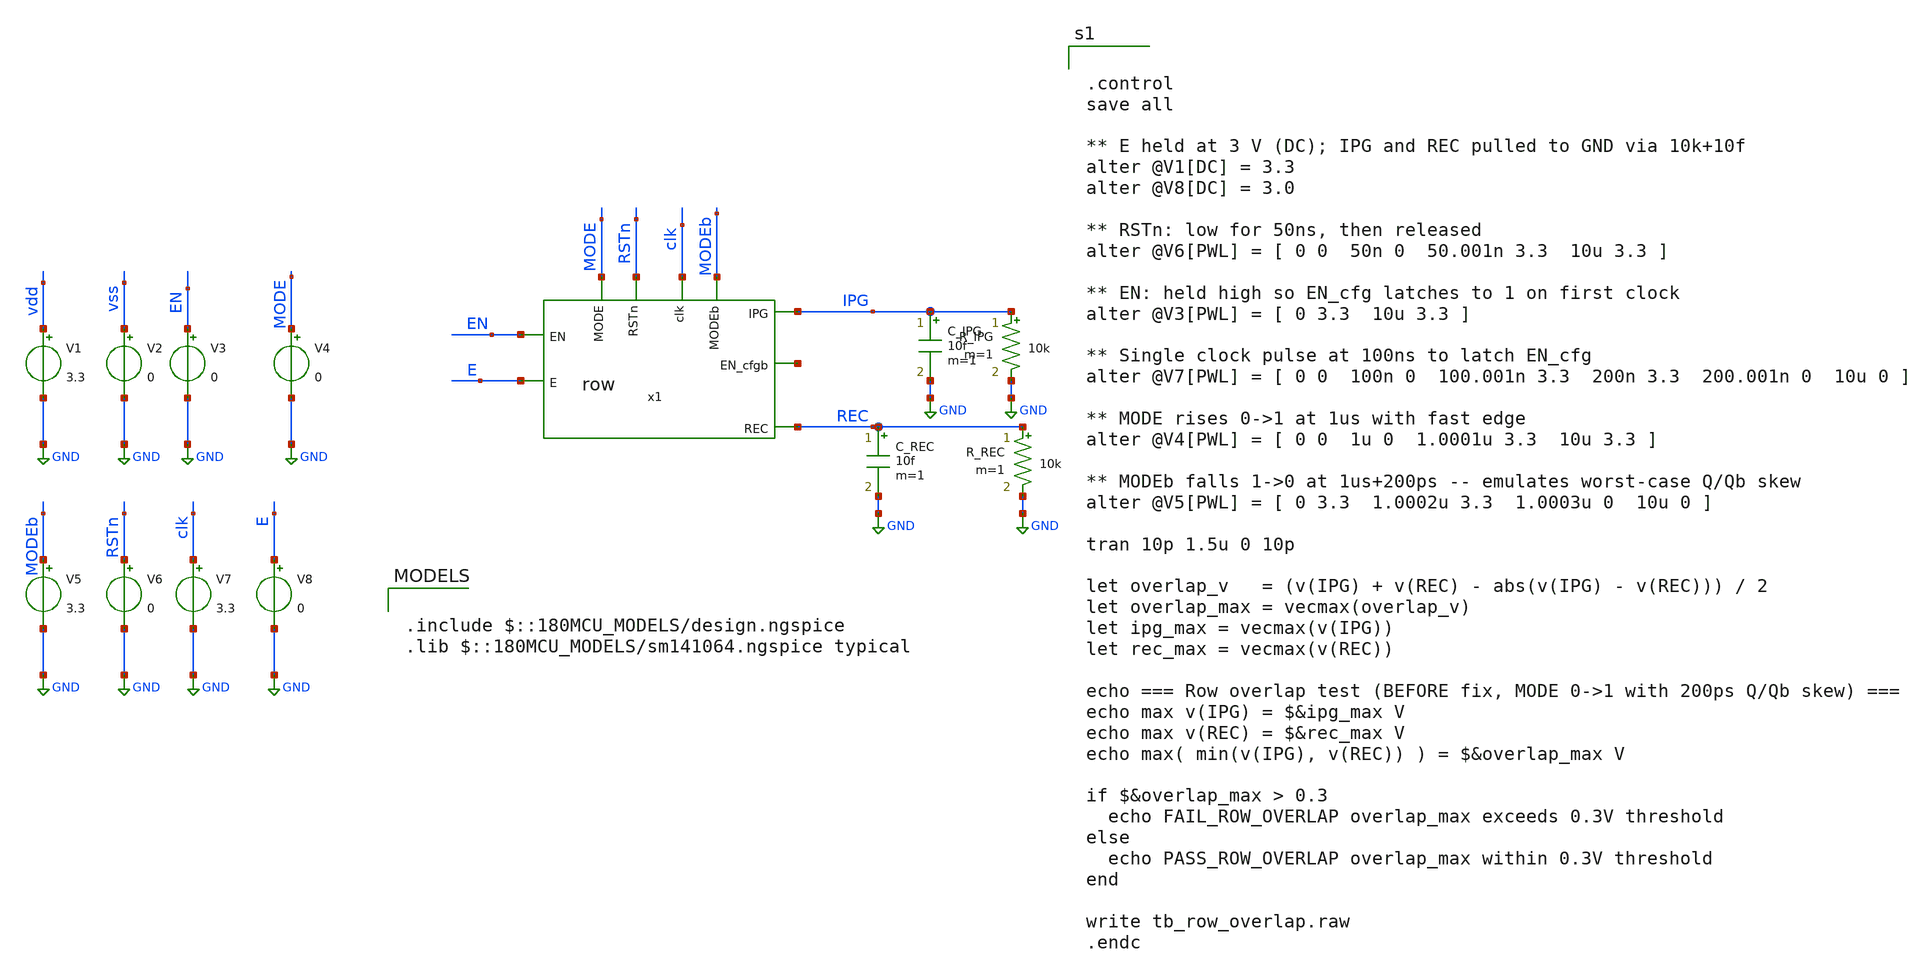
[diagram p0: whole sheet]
** sch_path: tb_row_overlap.sch
**.subckt tb_row_overlap
x1 IPG MODEb EN net1 clk E MODE RSTn REC row
V1 vdd GND 3.3
V2 vss GND 0
V3 EN GND 0
V4 MODE GND 0
V5 MODEb GND 3.3
V6 RSTn GND 0
V7 clk GND 3.3
V8 E GND 0
C_REC REC GND 10f m=1
C_IPG IPG GND 10f m=1
R_IPG IPG GND 10k m=1
R_REC REC GND 10k m=1
**** begin user architecture code

.include $::180MCU_MODELS/design.ngspice
.lib $::180MCU_MODELS/sm141064.ngspice typical



.control
save all

** E held at 3 V (DC); IPG and REC pulled to GND via 10k+10f
alter @V1[DC] = 3.3
alter @V8[DC] = 3.0

** RSTn: low for 50ns, then released
alter @V6[PWL] = [ 0 0  50n 0  50.001n 3.3  10u 3.3 ]

** EN: held high so EN_cfg latches to 1 on first clock
alter @V3[PWL] = [ 0 3.3  10u 3.3 ]

** Single clock pulse at 100ns to latch EN_cfg
alter @V7[PWL] = [ 0 0  100n 0  100.001n 3.3  200n 3.3  200.001n 0  10u 0 ]

** MODE rises 0->1 at 1us with fast edge
alter @V4[PWL] = [ 0 0  1u 0  1.0001u 3.3  10u 3.3 ]

** MODEb falls 1->0 at 1us+200ps -- emulates worst-case Q/Qb skew
alter @V5[PWL] = [ 0 3.3  1.0002u 3.3  1.0003u 0  10u 0 ]

tran 10p 1.5u 0 10p

let overlap_v   = (v(IPG) + v(REC) - abs(v(IPG) - v(REC))) / 2
let overlap_max = vecmax(overlap_v)
let ipg_max = vecmax(v(IPG))
let rec_max = vecmax(v(REC))

echo === Row overlap test (BEFORE fix, MODE 0->1 with 200ps Q/Qb skew) ===
echo max v(IPG) = $&ipg_max V
echo max v(REC) = $&rec_max V
echo max( min(v(IPG), v(REC)) ) = $&overlap_max V

if $&overlap_max > 0.3
  echo FAIL_ROW_OVERLAP overlap_max exceeds 0.3V threshold
else
  echo PASS_ROW_OVERLAP overlap_max within 0.3V threshold
end

write tb_row_overlap.raw
.endc


**** end user architecture code
**.ends

* expanding   symbol:  row.sym # of pins=9
** sym_path: row.sym
** sch_path: row.sch
.subckt row IPG MODEb EN EN_cfgb clk E MODE RSTn REC
*.ipin EN
*.ipin clk
*.ipin MODEb
*.ipin MODE
*.ipin E
*.opin IPG
*.opin REC
*.ipin RSTn
*.opin EN_cfgb
x1 EN_cfg SW_IPG MODEb AND
x2 vdd RSTn EN EN_cfg EN_cfgb clk GND DFF
x3 IPG SW_IPG SW_IPGb E TGATE
x4 EN_cfg SW_REC MODE AND
x6 REC SW_REC SW_RECb E TGATE
x5 SW_IPGb SW_IPG INV
x7 SW_RECb SW_REC INV
.ends


* expanding   symbol:  AND/AND.sym # of pins=3
** sym_path: AND/AND.sym
** sch_path: AND/AND.sch
.subckt AND IN0 OUT IN1
*.opin OUT
*.ipin IN0
*.ipin IN1
XM1 net1 IN0 net2 GND nfet_03v3 L=0.28u W=1u nf=1 ad='int((nf+1)/2) * W/nf * 0.18u' as='int((nf+2)/2) * W/nf * 0.18u'
+ pd='2*int((nf+1)/2) * (W/nf + 0.18u)' ps='2*int((nf+2)/2) * (W/nf + 0.18u)' nrd='0.18u / W' nrs='0.18u / W'
+ sa=0 sb=0 sd=0 m=1
XM2 net2 IN1 GND GND nfet_03v3 L=0.28u W=1u nf=1 ad='int((nf+1)/2) * W/nf * 0.18u' as='int((nf+2)/2) * W/nf * 0.18u'
+ pd='2*int((nf+1)/2) * (W/nf + 0.18u)' ps='2*int((nf+2)/2) * (W/nf + 0.18u)' nrd='0.18u / W' nrs='0.18u / W'
+ sa=0 sb=0 sd=0 m=1
XM3 net1 IN0 vdd vdd pfet_03v3 L=0.28u W=1u nf=1 ad='int((nf+1)/2) * W/nf * 0.18u' as='int((nf+2)/2) * W/nf * 0.18u'
+ pd='2*int((nf+1)/2) * (W/nf + 0.18u)' ps='2*int((nf+2)/2) * (W/nf + 0.18u)' nrd='0.18u / W' nrs='0.18u / W'
+ sa=0 sb=0 sd=0 m=1
XM4 net1 IN1 vdd vdd pfet_03v3 L=0.28u W=1u nf=1 ad='int((nf+1)/2) * W/nf * 0.18u' as='int((nf+2)/2) * W/nf * 0.18u'
+ pd='2*int((nf+1)/2) * (W/nf + 0.18u)' ps='2*int((nf+2)/2) * (W/nf + 0.18u)' nrd='0.18u / W' nrs='0.18u / W'
+ sa=0 sb=0 sd=0 m=1
x1 OUT net1 INV
.ends


* expanding   symbol:  DFF/DFF.sym # of pins=7
** sym_path: DFF/DFF.sym
** sch_path: DFF/DFF.sch
.subckt DFF vdd RSTn D Q Qb CLK vss
*.ipin D
*.ipin CLK
*.ipin RSTn
*.opin Q
*.iopin vdd
*.iopin vss
*.opin Qb
XM1 net1 D net3 vss nfet_03v3 L=0.28u W=1u nf=1 ad='int((nf+1)/2) * W/nf * 0.18u' as='int((nf+2)/2) * W/nf * 0.18u'
+ pd='2*int((nf+1)/2) * (W/nf + 0.18u)' ps='2*int((nf+2)/2) * (W/nf + 0.18u)' nrd='0.18u / W' nrs='0.18u / W'
+ sa=0 sb=0 sd=0 m=1
XM2 net1 D net2 vdd pfet_03v3 L=0.28u W=1u nf=1 ad='int((nf+1)/2) * W/nf * 0.18u' as='int((nf+2)/2) * W/nf * 0.18u'
+ pd='2*int((nf+1)/2) * (W/nf + 0.18u)' ps='2*int((nf+2)/2) * (W/nf + 0.18u)' nrd='0.18u / W' nrs='0.18u / W'
+ sa=0 sb=0 sd=0 m=1
XM3 net2 c vdd vdd pfet_03v3 L=0.28u W=1u nf=1 ad='int((nf+1)/2) * W/nf * 0.18u' as='int((nf+2)/2) * W/nf * 0.18u'
+ pd='2*int((nf+1)/2) * (W/nf + 0.18u)' ps='2*int((nf+2)/2) * (W/nf + 0.18u)' nrd='0.18u / W' nrs='0.18u / W'
+ sa=0 sb=0 sd=0 m=1
XM4 net3 cbar vss vss nfet_03v3 L=0.28u W=1u nf=1 ad='int((nf+1)/2) * W/nf * 0.18u' as='int((nf+2)/2) * W/nf * 0.18u'
+ pd='2*int((nf+1)/2) * (W/nf + 0.18u)' ps='2*int((nf+2)/2) * (W/nf + 0.18u)' nrd='0.18u / W' nrs='0.18u / W'
+ sa=0 sb=0 sd=0 m=1
XM5 cbar CLK vss vss nfet_03v3 L=0.28u W=1u nf=1 ad='int((nf+1)/2) * W/nf * 0.18u' as='int((nf+2)/2) * W/nf * 0.18u'
+ pd='2*int((nf+1)/2) * (W/nf + 0.18u)' ps='2*int((nf+2)/2) * (W/nf + 0.18u)' nrd='0.18u / W' nrs='0.18u / W'
+ sa=0 sb=0 sd=0 m=1
XM6 cbar CLK vdd vdd pfet_03v3 L=0.28u W=1u nf=1 ad='int((nf+1)/2) * W/nf * 0.18u' as='int((nf+2)/2) * W/nf * 0.18u'
+ pd='2*int((nf+1)/2) * (W/nf + 0.18u)' ps='2*int((nf+2)/2) * (W/nf + 0.18u)' nrd='0.18u / W' nrs='0.18u / W'
+ sa=0 sb=0 sd=0 m=1
XM7 c cbar vss vss nfet_03v3 L=0.28u W=1u nf=1 ad='int((nf+1)/2) * W/nf * 0.18u' as='int((nf+2)/2) * W/nf * 0.18u'
+ pd='2*int((nf+1)/2) * (W/nf + 0.18u)' ps='2*int((nf+2)/2) * (W/nf + 0.18u)' nrd='0.18u / W' nrs='0.18u / W'
+ sa=0 sb=0 sd=0 m=1
XM8 c cbar vdd vdd pfet_03v3 L=0.28u W=1u nf=1 ad='int((nf+1)/2) * W/nf * 0.18u' as='int((nf+2)/2) * W/nf * 0.18u'
+ pd='2*int((nf+1)/2) * (W/nf + 0.18u)' ps='2*int((nf+2)/2) * (W/nf + 0.18u)' nrd='0.18u / W' nrs='0.18u / W'
+ sa=0 sb=0 sd=0 m=1
XM11 net5 RSTn net4 vss nfet_03v3 L=0.28u W=1u nf=1 ad='int((nf+1)/2) * W/nf * 0.18u' as='int((nf+2)/2) * W/nf * 0.18u'
+ pd='2*int((nf+1)/2) * (W/nf + 0.18u)' ps='2*int((nf+2)/2) * (W/nf + 0.18u)' nrd='0.18u / W' nrs='0.18u / W'
+ sa=0 sb=0 sd=0 m=1
XM12 net4 net6 vss vss nfet_03v3 L=0.28u W=1u nf=1 ad='int((nf+1)/2) * W/nf * 0.18u' as='int((nf+2)/2) * W/nf * 0.18u'
+ pd='2*int((nf+1)/2) * (W/nf + 0.18u)' ps='2*int((nf+2)/2) * (W/nf + 0.18u)' nrd='0.18u / W' nrs='0.18u / W'
+ sa=0 sb=0 sd=0 m=1
XM13 net5 RSTn vdd vdd pfet_03v3 L=0.28u W=1u nf=1 ad='int((nf+1)/2) * W/nf * 0.18u' as='int((nf+2)/2) * W/nf * 0.18u'
+ pd='2*int((nf+1)/2) * (W/nf + 0.18u)' ps='2*int((nf+2)/2) * (W/nf + 0.18u)' nrd='0.18u / W' nrs='0.18u / W'
+ sa=0 sb=0 sd=0 m=1
XM14 net5 net6 vdd vdd pfet_03v3 L=0.28u W=1u nf=1 ad='int((nf+1)/2) * W/nf * 0.18u' as='int((nf+2)/2) * W/nf * 0.18u'
+ pd='2*int((nf+1)/2) * (W/nf + 0.18u)' ps='2*int((nf+2)/2) * (W/nf + 0.18u)' nrd='0.18u / W' nrs='0.18u / W'
+ sa=0 sb=0 sd=0 m=1
XM15 net6 net1 vss vss nfet_03v3 L=0.28u W=1u nf=1 ad='int((nf+1)/2) * W/nf * 0.18u' as='int((nf+2)/2) * W/nf * 0.18u'
+ pd='2*int((nf+1)/2) * (W/nf + 0.18u)' ps='2*int((nf+2)/2) * (W/nf + 0.18u)' nrd='0.18u / W' nrs='0.18u / W'
+ sa=0 sb=0 sd=0 m=1
XM16 net6 net1 vdd vdd pfet_03v3 L=0.28u W=1u nf=1 ad='int((nf+1)/2) * W/nf * 0.18u' as='int((nf+2)/2) * W/nf * 0.18u'
+ pd='2*int((nf+1)/2) * (W/nf + 0.18u)' ps='2*int((nf+2)/2) * (W/nf + 0.18u)' nrd='0.18u / W' nrs='0.18u / W'
+ sa=0 sb=0 sd=0 m=1
XM21 net9 net7 net8 vss nfet_03v3 L=0.28u W=1u nf=1 ad='int((nf+1)/2) * W/nf * 0.18u' as='int((nf+2)/2) * W/nf * 0.18u'
+ pd='2*int((nf+1)/2) * (W/nf + 0.18u)' ps='2*int((nf+2)/2) * (W/nf + 0.18u)' nrd='0.18u / W' nrs='0.18u / W'
+ sa=0 sb=0 sd=0 m=1
XM22 net8 RSTn vss vss nfet_03v3 L=0.28u W=1u nf=1 ad='int((nf+1)/2) * W/nf * 0.18u' as='int((nf+2)/2) * W/nf * 0.18u'
+ pd='2*int((nf+1)/2) * (W/nf + 0.18u)' ps='2*int((nf+2)/2) * (W/nf + 0.18u)' nrd='0.18u / W' nrs='0.18u / W'
+ sa=0 sb=0 sd=0 m=1
XM23 net9 net7 vdd vdd pfet_03v3 L=0.28u W=1u nf=1 ad='int((nf+1)/2) * W/nf * 0.18u' as='int((nf+2)/2) * W/nf * 0.18u'
+ pd='2*int((nf+1)/2) * (W/nf + 0.18u)' ps='2*int((nf+2)/2) * (W/nf + 0.18u)' nrd='0.18u / W' nrs='0.18u / W'
+ sa=0 sb=0 sd=0 m=1
XM24 net9 RSTn vdd vdd pfet_03v3 L=0.28u W=1u nf=1 ad='int((nf+1)/2) * W/nf * 0.18u' as='int((nf+2)/2) * W/nf * 0.18u'
+ pd='2*int((nf+1)/2) * (W/nf + 0.18u)' ps='2*int((nf+2)/2) * (W/nf + 0.18u)' nrd='0.18u / W' nrs='0.18u / W'
+ sa=0 sb=0 sd=0 m=1
XM25 Q net9 vss vss nfet_03v3 L=0.28u W=1u nf=1 ad='int((nf+1)/2) * W/nf * 0.18u' as='int((nf+2)/2) * W/nf * 0.18u'
+ pd='2*int((nf+1)/2) * (W/nf + 0.18u)' ps='2*int((nf+2)/2) * (W/nf + 0.18u)' nrd='0.18u / W' nrs='0.18u / W'
+ sa=0 sb=0 sd=0 m=1
XM26 Q net9 vdd vdd pfet_03v3 L=0.28u W=1u nf=1 ad='int((nf+1)/2) * W/nf * 0.18u' as='int((nf+2)/2) * W/nf * 0.18u'
+ pd='2*int((nf+1)/2) * (W/nf + 0.18u)' ps='2*int((nf+2)/2) * (W/nf + 0.18u)' nrd='0.18u / W' nrs='0.18u / W'
+ sa=0 sb=0 sd=0 m=1
XM19 net7 net9 net11 vss nfet_03v3 L=0.28u W=1u nf=1 ad='int((nf+1)/2) * W/nf * 0.18u' as='int((nf+2)/2) * W/nf * 0.18u'
+ pd='2*int((nf+1)/2) * (W/nf + 0.18u)' ps='2*int((nf+2)/2) * (W/nf + 0.18u)' nrd='0.18u / W' nrs='0.18u / W'
+ sa=0 sb=0 sd=0 m=1
XM20 net7 net9 net10 vdd pfet_03v3 L=0.28u W=1u nf=1 ad='int((nf+1)/2) * W/nf * 0.18u' as='int((nf+2)/2) * W/nf * 0.18u'
+ pd='2*int((nf+1)/2) * (W/nf + 0.18u)' ps='2*int((nf+2)/2) * (W/nf + 0.18u)' nrd='0.18u / W' nrs='0.18u / W'
+ sa=0 sb=0 sd=0 m=1
XM31 net10 c vdd vdd pfet_03v3 L=0.28u W=1u nf=1 ad='int((nf+1)/2) * W/nf * 0.18u' as='int((nf+2)/2) * W/nf * 0.18u'
+ pd='2*int((nf+1)/2) * (W/nf + 0.18u)' ps='2*int((nf+2)/2) * (W/nf + 0.18u)' nrd='0.18u / W' nrs='0.18u / W'
+ sa=0 sb=0 sd=0 m=1
XM32 net11 cbar vss vss nfet_03v3 L=0.28u W=1u nf=1 ad='int((nf+1)/2) * W/nf * 0.18u' as='int((nf+2)/2) * W/nf * 0.18u'
+ pd='2*int((nf+1)/2) * (W/nf + 0.18u)' ps='2*int((nf+2)/2) * (W/nf + 0.18u)' nrd='0.18u / W' nrs='0.18u / W'
+ sa=0 sb=0 sd=0 m=1
XM35 net12 net9 vss vss nfet_03v3 L=0.28u W=1u nf=1 ad='int((nf+1)/2) * W/nf * 0.18u' as='int((nf+2)/2) * W/nf * 0.18u'
+ pd='2*int((nf+1)/2) * (W/nf + 0.18u)' ps='2*int((nf+2)/2) * (W/nf + 0.18u)' nrd='0.18u / W' nrs='0.18u / W'
+ sa=0 sb=0 sd=0 m=1
XM36 net12 net9 vdd vdd pfet_03v3 L=0.28u W=1u nf=1 ad='int((nf+1)/2) * W/nf * 0.18u' as='int((nf+2)/2) * W/nf * 0.18u'
+ pd='2*int((nf+1)/2) * (W/nf + 0.18u)' ps='2*int((nf+2)/2) * (W/nf + 0.18u)' nrd='0.18u / W' nrs='0.18u / W'
+ sa=0 sb=0 sd=0 m=1
XM37 Qb net12 vss vss nfet_03v3 L=0.28u W=1u nf=1 ad='int((nf+1)/2) * W/nf * 0.18u' as='int((nf+2)/2) * W/nf * 0.18u'
+ pd='2*int((nf+1)/2) * (W/nf + 0.18u)' ps='2*int((nf+2)/2) * (W/nf + 0.18u)' nrd='0.18u / W' nrs='0.18u / W'
+ sa=0 sb=0 sd=0 m=1
XM38 Qb net12 vdd vdd pfet_03v3 L=0.28u W=1u nf=1 ad='int((nf+1)/2) * W/nf * 0.18u' as='int((nf+2)/2) * W/nf * 0.18u'
+ pd='2*int((nf+1)/2) * (W/nf + 0.18u)' ps='2*int((nf+2)/2) * (W/nf + 0.18u)' nrd='0.18u / W' nrs='0.18u / W'
+ sa=0 sb=0 sd=0 m=1
XM9 net1 c net5 vss nfet_03v3 L=0.28u W=1u nf=1 ad='int((nf+1)/2) * W/nf * 0.18u' as='int((nf+2)/2) * W/nf * 0.18u'
+ pd='2*int((nf+1)/2) * (W/nf + 0.18u)' ps='2*int((nf+2)/2) * (W/nf + 0.18u)' nrd='0.18u / W' nrs='0.18u / W'
+ sa=0 sb=0 sd=0 m=1
XM10 net1 cbar net5 vdd pfet_03v3 L=0.28u W=1u nf=1 ad='int((nf+1)/2) * W/nf * 0.18u' as='int((nf+2)/2) * W/nf * 0.18u'
+ pd='2*int((nf+1)/2) * (W/nf + 0.18u)' ps='2*int((nf+2)/2) * (W/nf + 0.18u)' nrd='0.18u / W' nrs='0.18u / W'
+ sa=0 sb=0 sd=0 m=1
XM17 net6 c net7 vss nfet_03v3 L=0.28u W=1u nf=1 ad='int((nf+1)/2) * W/nf * 0.18u' as='int((nf+2)/2) * W/nf * 0.18u'
+ pd='2*int((nf+1)/2) * (W/nf + 0.18u)' ps='2*int((nf+2)/2) * (W/nf + 0.18u)' nrd='0.18u / W' nrs='0.18u / W'
+ sa=0 sb=0 sd=0 m=1
XM18 net6 cbar net7 vdd pfet_03v3 L=0.28u W=1u nf=1 ad='int((nf+1)/2) * W/nf * 0.18u' as='int((nf+2)/2) * W/nf * 0.18u'
+ pd='2*int((nf+1)/2) * (W/nf + 0.18u)' ps='2*int((nf+2)/2) * (W/nf + 0.18u)' nrd='0.18u / W' nrs='0.18u / W'
+ sa=0 sb=0 sd=0 m=1
.ends


* expanding   symbol:  TGATE/TGATE.sym # of pins=4
** sym_path: TGATE/TGATE.sym
** sch_path: TGATE/TGATE.sch
.subckt TGATE out c cbar in
*.ipin in
*.opin out
*.ipin cbar
*.ipin c
XM1 out cbar in VDD pfet_03v3 L=0.28u W=1u nf=1 ad='int((nf+1)/2) * W/nf * 0.18u' as='int((nf+2)/2) * W/nf * 0.18u'
+ pd='2*int((nf+1)/2) * (W/nf + 0.18u)' ps='2*int((nf+2)/2) * (W/nf + 0.18u)' nrd='0.18u / W' nrs='0.18u / W'
+ sa=0 sb=0 sd=0 m=1
XM2 out c in GND nfet_03v3 L=0.28u W=1u nf=1 ad='int((nf+1)/2) * W/nf * 0.18u' as='int((nf+2)/2) * W/nf * 0.18u'
+ pd='2*int((nf+1)/2) * (W/nf + 0.18u)' ps='2*int((nf+2)/2) * (W/nf + 0.18u)' nrd='0.18u / W' nrs='0.18u / W'
+ sa=0 sb=0 sd=0 m=1
.ends


* expanding   symbol:  AND/INV.sym # of pins=2
** sym_path: AND/INV.sym
** sch_path: AND/INV.sch
.subckt INV OUT IN
*.ipin IN
*.opin OUT
XM1 OUT IN VDD VDD pfet_03v3 L=0.28u W=1u nf=1 ad='int((nf+1)/2) * W/nf * 0.18u' as='int((nf+2)/2) * W/nf * 0.18u'
+ pd='2*int((nf+1)/2) * (W/nf + 0.18u)' ps='2*int((nf+2)/2) * (W/nf + 0.18u)' nrd='0.18u / W' nrs='0.18u / W'
+ sa=0 sb=0 sd=0 m=1
XM2 OUT IN GND GND nfet_03v3 L=0.28u W=0.5u nf=1 ad='int((nf+1)/2) * W/nf * 0.18u' as='int((nf+2)/2) * W/nf * 0.18u'
+ pd='2*int((nf+1)/2) * (W/nf + 0.18u)' ps='2*int((nf+2)/2) * (W/nf + 0.18u)' nrd='0.18u / W' nrs='0.18u / W'
+ sa=0 sb=0 sd=0 m=1
.ends

.GLOBAL GND
.GLOBAL vdd
.GLOBAL VDD
.end
